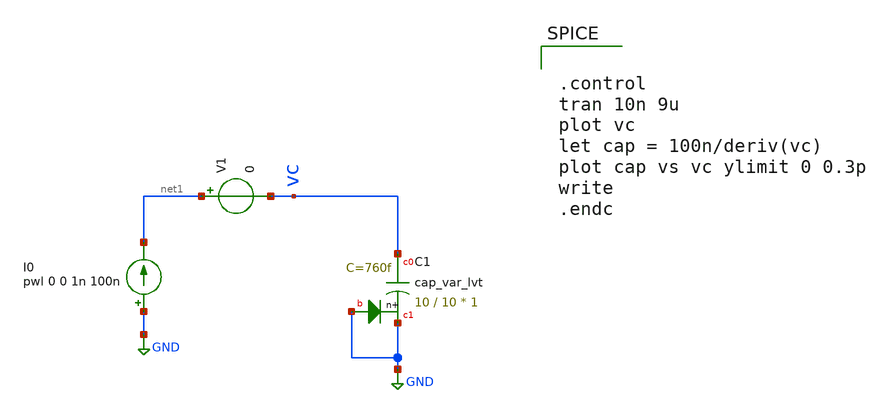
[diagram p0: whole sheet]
** sch_path: varactor_meas/varactor_tran.sch
**.subckt varactor_tran
XC1 vc GND GND sky130_fd_pr__cap_var_lvt W=10 L=10 VM=1 m=1
I0 GND net1 pwl 0 0 1n 100n
V1 net1 vc 0
**** begin user architecture code


.control
tran 10n 9u
plot vc
let cap = 100n/deriv(vc)
plot cap vs vc ylimit 0 0.3p
write
.endc




.option wnflag = 1
.lib /usr/local/share/pdk/sky130A/libs.tech/ngspice/sky130.lib.spice tt
.include /usr/local/share/pdk/sky130A/libs.ref/sky130_fd_pr/spice/sky130_fd_pr__ind_05_220.model.spice
.param mc_mm_switch=0


**** end user architecture code
**.ends
.GLOBAL GND
.end
